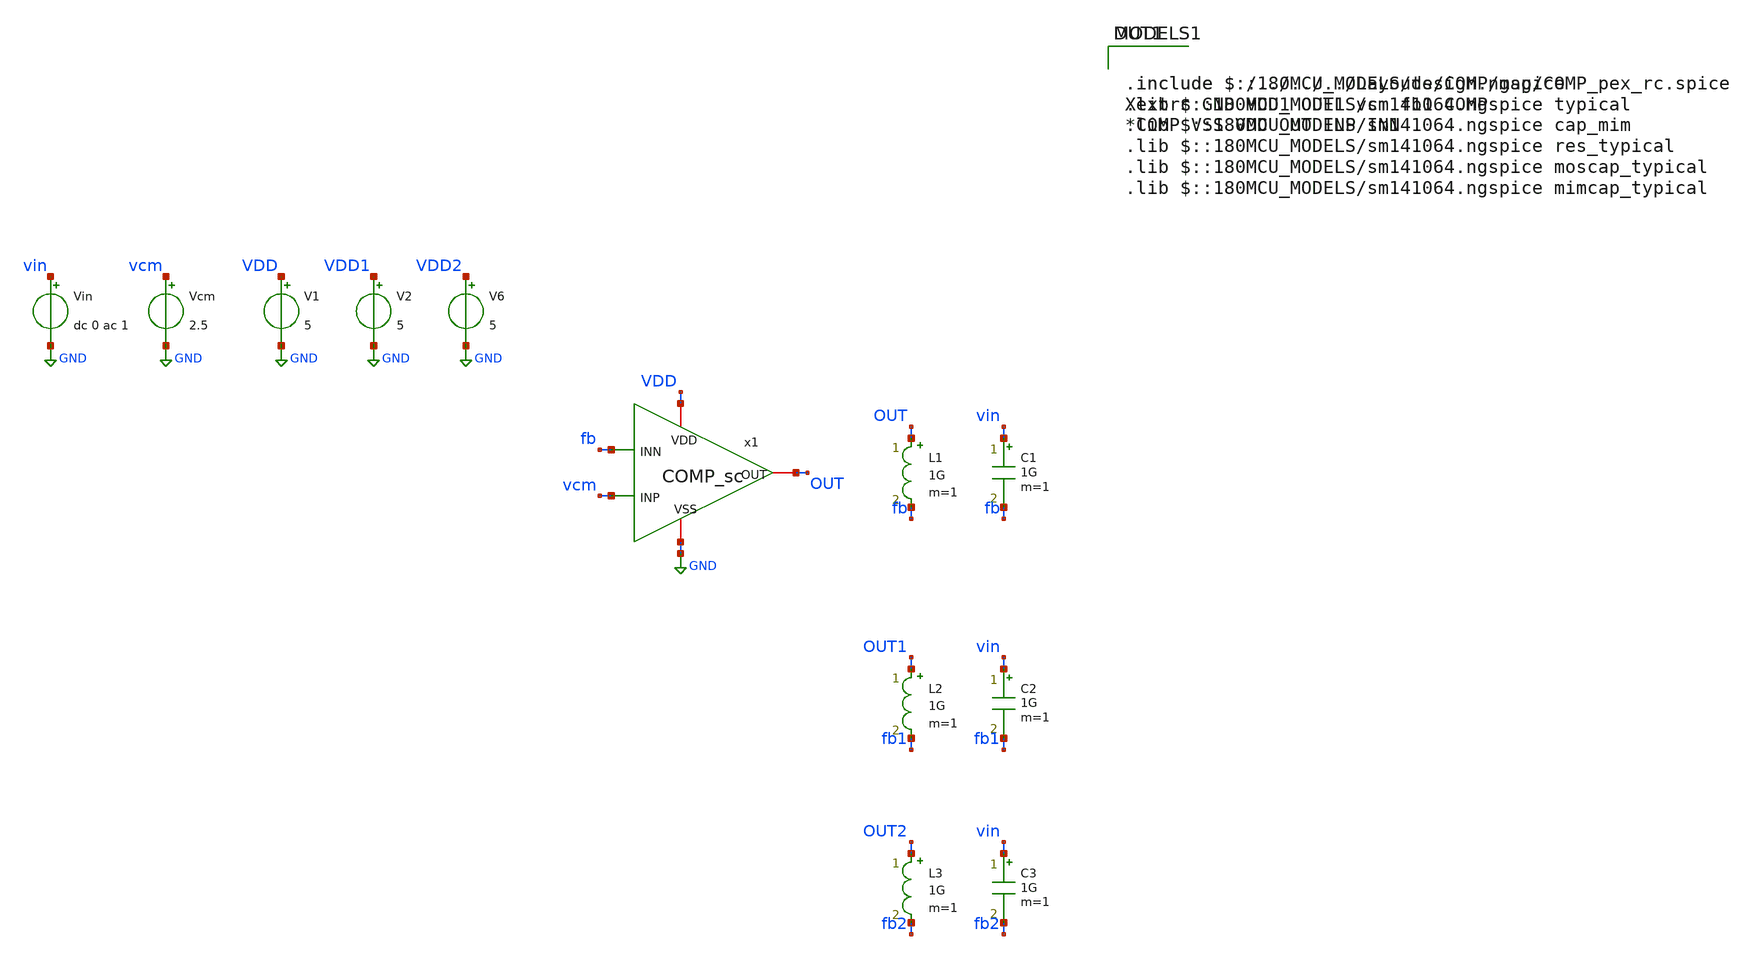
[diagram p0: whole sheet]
** sch_path: FINAL/XSCHEM/TEST/test_comp_ac.sch
**.subckt test_comp_ac
V1 VDD GND 5
V2 VDD1 GND 5
Vin vin GND dc 0 ac 1
Vcm vcm GND 2.5
x1 VDD fb OUT vcm GND COMP_sc
L1 OUT fb 1G m=1
C1 vin fb 1G m=1
L2 OUT1 fb1 1G m=1
C2 vin fb1 1G m=1
L3 OUT2 fb2 1G m=1
C3 vin fb2 1G m=1
V6 VDD2 GND 5
**** begin user architecture code

.include $::180MCU_MODELS/design.ngspice
.lib $::180MCU_MODELS/sm141064.ngspice typical
.lib $::180MCU_MODELS/sm141064.ngspice cap_mim
.lib $::180MCU_MODELS/sm141064.ngspice res_typical
.lib $::180MCU_MODELS/sm141064.ngspice moscap_typical
.lib $::180MCU_MODELS/sm141064.ngspice mimcap_typical


.include ../../../../Layouts/COMP/mag/COMP_pex_rc.spice
Xextrc GND VDD1 OUT1 vcm fb1 COMP
*COMP VSS VDD OUT INP INN


* The v2 layout, with its own self-biasing loop (L3/C3, node fb2) and its own
* supply, so it can be measured just like v1.
.include ../../../../layouts_v2/COMP/mag/COMP_V2_pex_rc.spice
Xextrc2 GND VDD2 OUT2 vcm fb2 COMP_V2



* CAREFUL: not one brace in this text. xschem counts them to find where the
* attribute block ends and a single one inside a comment cuts it in half,
* leaving the netlist with the template 'blabla' and raising no error.
*
* No se puede atar la entrada en continua y lanzar un .ac: el punto de
* operating point sits saturated and linearising there means nothing. Each branch
* lazo de L de 1 GH y C de 1 GF: en continua la L es un corto y el lazo unitario
* places the comparator at its own offset; in AC the L opens and the C
* shorts, and what is measured is the open-loop gain.
.save all
.control
ac dec 100 0.001 10G
wrdata ac.txt v(OUT) v(OUT1) v(OUT2)
.endc


**** end user architecture code
**.ends
.GLOBAL GND
.end
